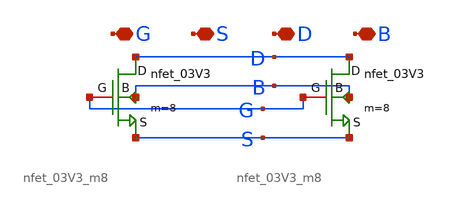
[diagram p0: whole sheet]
** sch_path: DAC_PAKISTAN_01/Pakistan1_Xschem/nfet_03V3_m16.sch
**.subckt nfet_03V3_m16 G S D B
*.iopin G
*.iopin S
*.iopin D
*.iopin B
x1 S D B G nfet_03V3_m8
x2 S D B G nfet_03V3_m8
**.ends
.end
